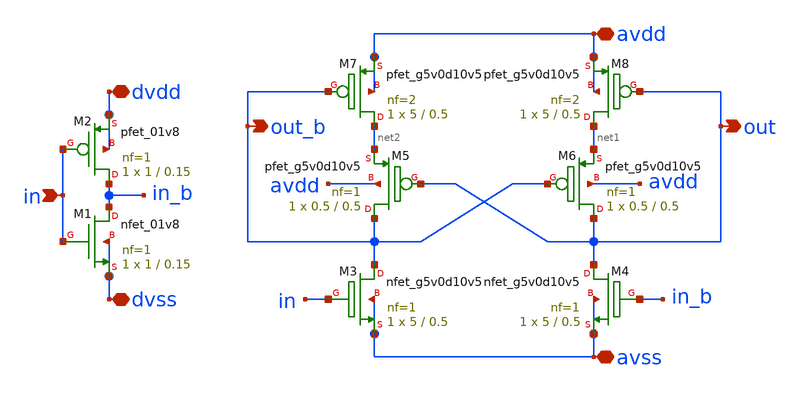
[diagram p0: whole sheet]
** sch_path: xschem/level_shift.sch
**.subckt level_shift in avdd avss dvss dvdd out out_b
*.ipin in
*.iopin avdd
*.iopin avss
*.iopin dvss
*.iopin dvdd
*.opin out
*.opin out_b
XM8 net1 out avdd avdd sky130_fd_pr__pfet_g5v0d10v5 L=0.5 W=5 nf=2 ad='int((nf+1)/2) * W/nf * 0.29' as='int((nf+2)/2) * W/nf * 0.29'
+ pd='2*int((nf+1)/2) * (W/nf + 0.29)' ps='2*int((nf+2)/2) * (W/nf + 0.29)' nrd='0.29 / W' nrs='0.29 / W'
+ sa=0 sb=0 sd=0 mult=1 m=1
XM4 out in_b avss avss sky130_fd_pr__nfet_g5v0d10v5 L=0.5 W=5 nf=1 ad='int((nf+1)/2) * W/nf * 0.29' as='int((nf+2)/2) * W/nf * 0.29'
+ pd='2*int((nf+1)/2) * (W/nf + 0.29)' ps='2*int((nf+2)/2) * (W/nf + 0.29)' nrd='0.29 / W' nrs='0.29 / W'
+ sa=0 sb=0 sd=0 mult=1 m=1
XM3 out_b in avss avss sky130_fd_pr__nfet_g5v0d10v5 L=0.5 W=5 nf=1 ad='int((nf+1)/2) * W/nf * 0.29' as='int((nf+2)/2) * W/nf * 0.29'
+ pd='2*int((nf+1)/2) * (W/nf + 0.29)' ps='2*int((nf+2)/2) * (W/nf + 0.29)' nrd='0.29 / W' nrs='0.29 / W'
+ sa=0 sb=0 sd=0 mult=1 m=1
XM5 out_b out net2 avdd sky130_fd_pr__pfet_g5v0d10v5 L=0.5 W=0.5 nf=1 ad='int((nf+1)/2) * W/nf * 0.29'
+ as='int((nf+2)/2) * W/nf * 0.29' pd='2*int((nf+1)/2) * (W/nf + 0.29)' ps='2*int((nf+2)/2) * (W/nf + 0.29)'
+ nrd='0.29 / W' nrs='0.29 / W' sa=0 sb=0 sd=0 mult=1 m=1
XM6 out out_b net1 avdd sky130_fd_pr__pfet_g5v0d10v5 L=0.5 W=0.5 nf=1 ad='int((nf+1)/2) * W/nf * 0.29'
+ as='int((nf+2)/2) * W/nf * 0.29' pd='2*int((nf+1)/2) * (W/nf + 0.29)' ps='2*int((nf+2)/2) * (W/nf + 0.29)'
+ nrd='0.29 / W' nrs='0.29 / W' sa=0 sb=0 sd=0 mult=1 m=1
XM2 in_b in dvdd dvdd sky130_fd_pr__pfet_01v8 L=0.15 W=1 nf=1 ad='int((nf+1)/2) * W/nf * 0.29' as='int((nf+2)/2) * W/nf * 0.29'
+ pd='2*int((nf+1)/2) * (W/nf + 0.29)' ps='2*int((nf+2)/2) * (W/nf + 0.29)' nrd='0.29 / W' nrs='0.29 / W'
+ sa=0 sb=0 sd=0 mult=1 m=1
XM1 in_b in dvss dvss sky130_fd_pr__nfet_01v8 L=0.15 W=1 nf=1 ad='int((nf+1)/2) * W/nf * 0.29' as='int((nf+2)/2) * W/nf * 0.29'
+ pd='2*int((nf+1)/2) * (W/nf + 0.29)' ps='2*int((nf+2)/2) * (W/nf + 0.29)' nrd='0.29 / W' nrs='0.29 / W'
+ sa=0 sb=0 sd=0 mult=1 m=1
XM7 net2 out_b avdd avdd sky130_fd_pr__pfet_g5v0d10v5 L=0.5 W=5 nf=2 ad='int((nf+1)/2) * W/nf * 0.29'
+ as='int((nf+2)/2) * W/nf * 0.29' pd='2*int((nf+1)/2) * (W/nf + 0.29)' ps='2*int((nf+2)/2) * (W/nf + 0.29)'
+ nrd='0.29 / W' nrs='0.29 / W' sa=0 sb=0 sd=0 mult=1 m=1
**.ends
.end
